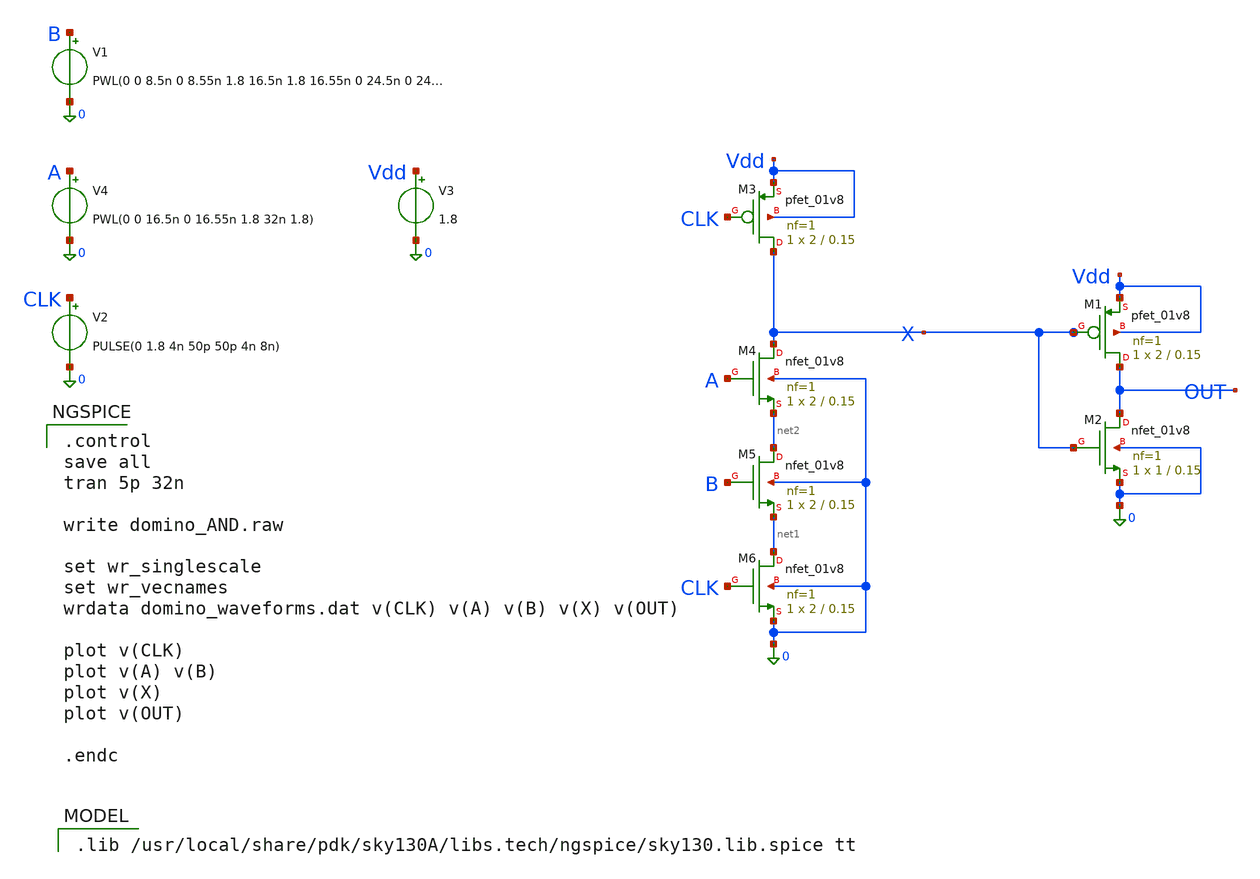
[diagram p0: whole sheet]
** sch_path: domino_AND.sch
**.subckt domino_AND
XM1 OUT X Vdd Vdd sky130_fd_pr__pfet_01v8 L=0.15 W=2 nf=1 ad='int((1 + 1)/2) * 2 / 1 * 0.29' as='int((1 + 2)/2) * 2 / 1 * 0.29'
+ pd='2*int((1 + 1)/2) * (2 / 1 + 0.29)' ps='2*int((1 + 2)/2) * (2 / 1 + 0.29)' nrd='0.29 / 2 ' nrs='0.29 / 2 '
+ sa=0 sb=0 sd=0 mult=1 m=1
XM2 OUT X 0 0 sky130_fd_pr__nfet_01v8 L=0.15 W=1 nf=1 ad='int((1 + 1)/2) * 1 / 1 * 0.29' as='int((1 + 2)/2) * 1 / 1 * 0.29'
+ pd='2*int((1 + 1)/2) * (1 / 1 + 0.29)' ps='2*int((1 + 2)/2) * (1 / 1 + 0.29)' nrd='0.29 / 1 ' nrs='0.29 / 1 '
+ sa=0 sb=0 sd=0 mult=1 m=1
V2 CLK 0 PULSE(0 1.8 4n 50p 50p 4n 8n)
V3 Vdd 0 1.8
XM3 X CLK Vdd Vdd sky130_fd_pr__pfet_01v8 L=0.15 W=2 nf=1 ad='int((1 + 1)/2) * 2 / 1 * 0.29' as='int((1 + 2)/2) * 2 / 1 * 0.29'
+ pd='2*int((1 + 1)/2) * (2 / 1 + 0.29)' ps='2*int((1 + 2)/2) * (2 / 1 + 0.29)' nrd='0.29 / 2 ' nrs='0.29 / 2 '
+ sa=0 sb=0 sd=0 mult=1 m=1
XM4 X A net2 0 sky130_fd_pr__nfet_01v8 L=0.15 W=2 nf=1 ad='int((1 + 1)/2) * 2 / 1 * 0.29' as='int((1 + 2)/2) * 2 / 1 * 0.29'
+ pd='2*int((1 + 1)/2) * (2 / 1 + 0.29)' ps='2*int((1 + 2)/2) * (2 / 1 + 0.29)' nrd='0.29 / 2 ' nrs='0.29 / 2 '
+ sa=0 sb=0 sd=0 mult=1 m=1
XM5 net2 B net1 0 sky130_fd_pr__nfet_01v8 L=0.15 W=2 nf=1 ad='int((1 + 1)/2) * 2 / 1 * 0.29' as='int((1 + 2)/2) * 2 / 1 * 0.29'
+ pd='2*int((1 + 1)/2) * (2 / 1 + 0.29)' ps='2*int((1 + 2)/2) * (2 / 1 + 0.29)' nrd='0.29 / 2 ' nrs='0.29 / 2 '
+ sa=0 sb=0 sd=0 mult=1 m=1
XM6 net1 CLK 0 0 sky130_fd_pr__nfet_01v8 L=0.15 W=2 nf=1 ad='int((1 + 1)/2) * 2 / 1 * 0.29' as='int((1 + 2)/2) * 2 / 1 * 0.29'
+ pd='2*int((1 + 1)/2) * (2 / 1 + 0.29)' ps='2*int((1 + 2)/2) * (2 / 1 + 0.29)' nrd='0.29 / 2 ' nrs='0.29 / 2 '
+ sa=0 sb=0 sd=0 mult=1 m=1
V1 B 0 PWL(0 0 8.5n 0 8.55n 1.8 16.5n 1.8 16.55n 0 24.5n 0 24.55n 1.8 32n 1.8)
V4 A 0 PWL(0 0 16.5n 0 16.55n 1.8 32n 1.8)
**** begin user architecture code

.lib /usr/local/share/pdk/sky130A/libs.tech/ngspice/sky130.lib.spice tt


.control
save all
tran 5p 32n

write domino_AND.raw

set wr_singlescale
set wr_vecnames
wrdata domino_waveforms.dat v(CLK) v(A) v(B) v(X) v(OUT)

plot v(CLK)
plot v(A) v(B)
plot v(X)
plot v(OUT)

.endc

**** end user architecture code
**.ends
.end
